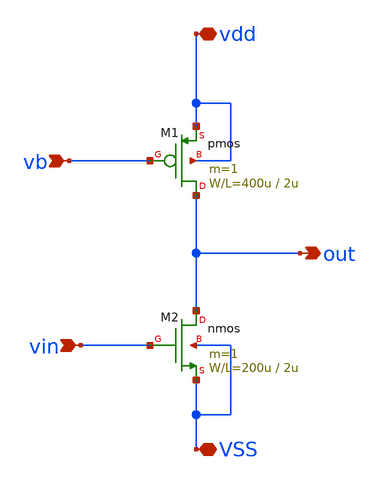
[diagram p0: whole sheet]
** sch_path: member_project/GroupWork/Team_Ando/ugeugeHigh/source_g.sch
**.subckt source_g vdd out vb vin VSS
*.iopin vdd
*.opin out
*.ipin vb
*.ipin vin
*.iopin VSS
M2 out vin VSS VSS nmos L=2u W=200u m=1
M1 out vb vdd vdd pmos L=2u W=400u m=1
**.ends
.end
